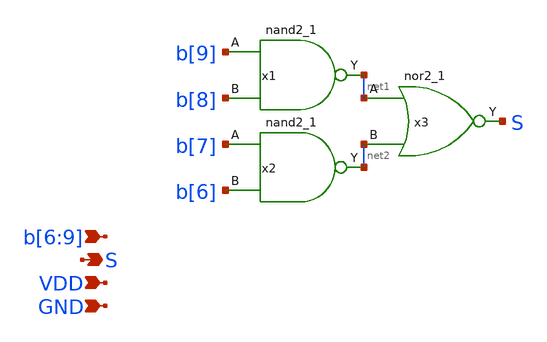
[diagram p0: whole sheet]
** sch_path: xschem/seg_selector_4_logic.sch
**.subckt seg_selector_4_logic S GND VDD b[6],b[7],b[8],b[9]
*.opin S
*.ipin GND
*.ipin VDD
*.ipin b[6],b[7],b[8],b[9]
x1 b[9] b[8] GND GND VDD VDD net1 sky130_fd_sc_hd__nand2_1
x2 b[7] b[6] GND GND VDD VDD net2 sky130_fd_sc_hd__nand2_1
x3 net1 net2 GND GND VDD VDD S sky130_fd_sc_hd__nor2_1
**.ends
.end
